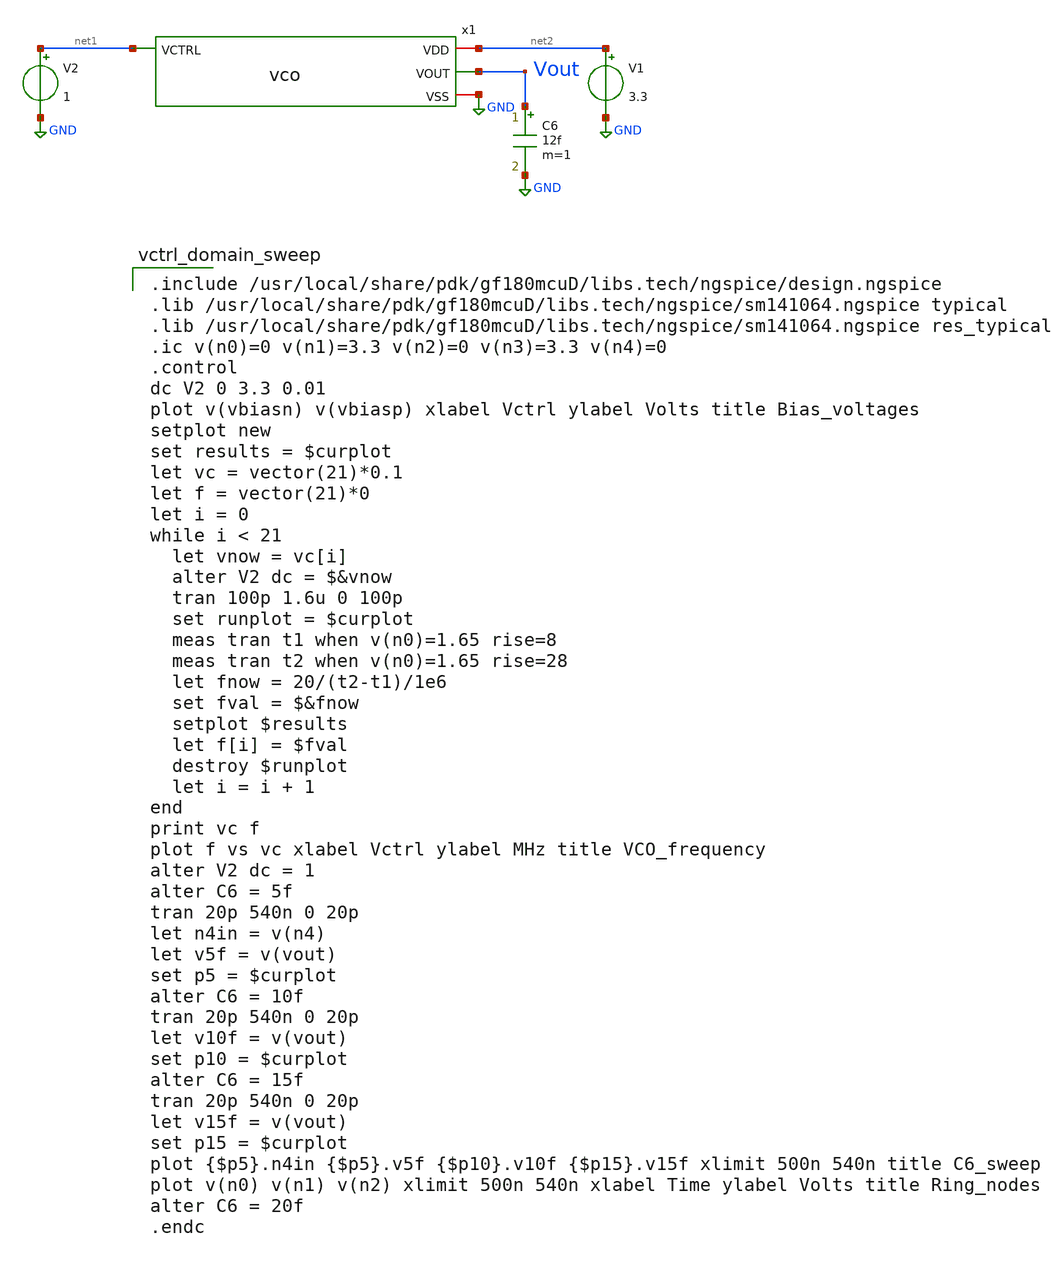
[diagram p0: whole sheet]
** sch_path: analog/vco/vco_tb.sch
**.subckt vco_tb
V1 net2 GND 3.3
V2 net1 GND 1
C6 Vout GND 12f m=1
x1 net2 net1 Vout GND vco
**** begin user architecture code

.include /usr/local/share/pdk/gf180mcuD/libs.tech/ngspice/design.ngspice
.lib /usr/local/share/pdk/gf180mcuD/libs.tech/ngspice/sm141064.ngspice typical
.lib /usr/local/share/pdk/gf180mcuD/libs.tech/ngspice/sm141064.ngspice res_typical
.ic v(n0)=0 v(n1)=3.3 v(n2)=0 v(n3)=3.3 v(n4)=0
.control
dc V2 0 3.3 0.01
plot v(vbiasn) v(vbiasp) xlabel Vctrl ylabel Volts title Bias_voltages
setplot new
set results = $curplot
let vc = vector(21)*0.1
let f = vector(21)*0
let i = 0
while i < 21
  let vnow = vc[i]
  alter V2 dc = $&vnow
  tran 100p 1.6u 0 100p
  set runplot = $curplot
  meas tran t1 when v(n0)=1.65 rise=8
  meas tran t2 when v(n0)=1.65 rise=28
  let fnow = 20/(t2-t1)/1e6
  set fval = $&fnow
  setplot $results
  let f[i] = $fval
  destroy $runplot
  let i = i + 1
end
print vc f
plot f vs vc xlabel Vctrl ylabel MHz title VCO_frequency
alter V2 dc = 1
alter C6 = 5f
tran 20p 540n 0 20p
let n4in = v(n4)
let v5f = v(vout)
set p5 = $curplot
alter C6 = 10f
tran 20p 540n 0 20p
let v10f = v(vout)
set p10 = $curplot
alter C6 = 15f
tran 20p 540n 0 20p
let v15f = v(vout)
set p15 = $curplot
plot {$p5}.n4in {$p5}.v5f {$p10}.v10f {$p15}.v15f xlimit 500n 540n title C6_sweep
plot v(n0) v(n1) v(n2) xlimit 500n 540n xlabel Time ylabel Volts title Ring_nodes
alter C6 = 20f
.endc


**** end user architecture code
**.ends

* expanding   symbol:  vco.sym # of pins=4
** sym_path: analog/vco/vco.sym
** sch_path: analog/vco/vco.sch
.subckt vco VDD VCTRL VOUT VSS
*.ipin VCTRL
*.iopin VDD
*.opin VOUT
*.iopin VSS
XM1 Vbiasn VCTRL net1 net1 pfet_03v3 L=1u W=8u nf=1 ad='int((nf+1)/2) * W/nf * 0.18u' as='int((nf+2)/2) * W/nf * 0.18u'
+ pd='2*int((nf+1)/2) * (W/nf + 0.18u)' ps='2*int((nf+2)/2) * (W/nf + 0.18u)' nrd='0.18u / W' nrs='0.18u / W'
+ sa=0 sb=0 sd=0 m=1
XM2 Vbiasn Vbiasn VSS VSS nfet_03v3 L=1u W=3u nf=1 ad='int((nf+1)/2) * W/nf * 0.18u' as='int((nf+2)/2) * W/nf * 0.18u'
+ pd='2*int((nf+1)/2) * (W/nf + 0.18u)' ps='2*int((nf+2)/2) * (W/nf + 0.18u)' nrd='0.18u / W' nrs='0.18u / W'
+ sa=0 sb=0 sd=0 m=1
XM3 Vbiasp Vbiasn VSS VSS nfet_03v3 L=1u W=3u nf=1 ad='int((nf+1)/2) * W/nf * 0.18u' as='int((nf+2)/2) * W/nf * 0.18u'
+ pd='2*int((nf+1)/2) * (W/nf + 0.18u)' ps='2*int((nf+2)/2) * (W/nf + 0.18u)' nrd='0.18u / W' nrs='0.18u / W'
+ sa=0 sb=0 sd=0 m=1
XM4 Vbiasp Vbiasp VDD VDD pfet_03v3 L=1u W=3u nf=1 ad='int((nf+1)/2) * W/nf * 0.18u' as='int((nf+2)/2) * W/nf * 0.18u'
+ pd='2*int((nf+1)/2) * (W/nf + 0.18u)' ps='2*int((nf+2)/2) * (W/nf + 0.18u)' nrd='0.18u / W' nrs='0.18u / W'
+ sa=0 sb=0 sd=0 m=1
XR1 net1 VDD VSS ppolyf_u r_width=1u r_length=189u m=1
XM5 net2 Vbiasn VSS VSS nfet_03v3 L=1u W=3u nf=1 ad='int((nf+1)/2) * W/nf * 0.18u' as='int((nf+2)/2) * W/nf * 0.18u'
+ pd='2*int((nf+1)/2) * (W/nf + 0.18u)' ps='2*int((nf+2)/2) * (W/nf + 0.18u)' nrd='0.18u / W' nrs='0.18u / W'
+ sa=0 sb=0 sd=0 m=1
XM6 n0 n4 net2 VSS nfet_03v3 L=0.28u W=1u nf=1 ad='int((nf+1)/2) * W/nf * 0.18u' as='int((nf+2)/2) * W/nf * 0.18u'
+ pd='2*int((nf+1)/2) * (W/nf + 0.18u)' ps='2*int((nf+2)/2) * (W/nf + 0.18u)' nrd='0.18u / W' nrs='0.18u / W'
+ sa=0 sb=0 sd=0 m=1
XM7 n0 n4 net3 VDD pfet_03v3 L=0.28u W=2u nf=1 ad='int((nf+1)/2) * W/nf * 0.18u' as='int((nf+2)/2) * W/nf * 0.18u'
+ pd='2*int((nf+1)/2) * (W/nf + 0.18u)' ps='2*int((nf+2)/2) * (W/nf + 0.18u)' nrd='0.18u / W' nrs='0.18u / W'
+ sa=0 sb=0 sd=0 m=1
XM8 net3 Vbiasp VDD VDD pfet_03v3 L=1u W=3u nf=1 ad='int((nf+1)/2) * W/nf * 0.18u' as='int((nf+2)/2) * W/nf * 0.18u'
+ pd='2*int((nf+1)/2) * (W/nf + 0.18u)' ps='2*int((nf+2)/2) * (W/nf + 0.18u)' nrd='0.18u / W' nrs='0.18u / W'
+ sa=0 sb=0 sd=0 m=1
XM9 net4 Vbiasn VSS VSS nfet_03v3 L=1u W=3u nf=1 ad='int((nf+1)/2) * W/nf * 0.18u' as='int((nf+2)/2) * W/nf * 0.18u'
+ pd='2*int((nf+1)/2) * (W/nf + 0.18u)' ps='2*int((nf+2)/2) * (W/nf + 0.18u)' nrd='0.18u / W' nrs='0.18u / W'
+ sa=0 sb=0 sd=0 m=1
XM10 n1 n0 net4 VSS nfet_03v3 L=0.28u W=1u nf=1 ad='int((nf+1)/2) * W/nf * 0.18u' as='int((nf+2)/2) * W/nf * 0.18u'
+ pd='2*int((nf+1)/2) * (W/nf + 0.18u)' ps='2*int((nf+2)/2) * (W/nf + 0.18u)' nrd='0.18u / W' nrs='0.18u / W'
+ sa=0 sb=0 sd=0 m=1
XM11 n1 n0 net5 VDD pfet_03v3 L=0.28u W=2u nf=1 ad='int((nf+1)/2) * W/nf * 0.18u' as='int((nf+2)/2) * W/nf * 0.18u'
+ pd='2*int((nf+1)/2) * (W/nf + 0.18u)' ps='2*int((nf+2)/2) * (W/nf + 0.18u)' nrd='0.18u / W' nrs='0.18u / W'
+ sa=0 sb=0 sd=0 m=1
XM12 net5 Vbiasp VDD VDD pfet_03v3 L=1u W=3u nf=1 ad='int((nf+1)/2) * W/nf * 0.18u' as='int((nf+2)/2) * W/nf * 0.18u'
+ pd='2*int((nf+1)/2) * (W/nf + 0.18u)' ps='2*int((nf+2)/2) * (W/nf + 0.18u)' nrd='0.18u / W' nrs='0.18u / W'
+ sa=0 sb=0 sd=0 m=1
XM13 net6 Vbiasn VSS VSS nfet_03v3 L=1u W=3u nf=1 ad='int((nf+1)/2) * W/nf * 0.18u' as='int((nf+2)/2) * W/nf * 0.18u'
+ pd='2*int((nf+1)/2) * (W/nf + 0.18u)' ps='2*int((nf+2)/2) * (W/nf + 0.18u)' nrd='0.18u / W' nrs='0.18u / W'
+ sa=0 sb=0 sd=0 m=1
XM14 n2 n1 net6 VSS nfet_03v3 L=0.28u W=1u nf=1 ad='int((nf+1)/2) * W/nf * 0.18u' as='int((nf+2)/2) * W/nf * 0.18u'
+ pd='2*int((nf+1)/2) * (W/nf + 0.18u)' ps='2*int((nf+2)/2) * (W/nf + 0.18u)' nrd='0.18u / W' nrs='0.18u / W'
+ sa=0 sb=0 sd=0 m=1
XM15 n2 n1 net7 VDD pfet_03v3 L=0.28u W=2u nf=1 ad='int((nf+1)/2) * W/nf * 0.18u' as='int((nf+2)/2) * W/nf * 0.18u'
+ pd='2*int((nf+1)/2) * (W/nf + 0.18u)' ps='2*int((nf+2)/2) * (W/nf + 0.18u)' nrd='0.18u / W' nrs='0.18u / W'
+ sa=0 sb=0 sd=0 m=1
XM16 net7 Vbiasp VDD VDD pfet_03v3 L=1u W=3u nf=1 ad='int((nf+1)/2) * W/nf * 0.18u' as='int((nf+2)/2) * W/nf * 0.18u'
+ pd='2*int((nf+1)/2) * (W/nf + 0.18u)' ps='2*int((nf+2)/2) * (W/nf + 0.18u)' nrd='0.18u / W' nrs='0.18u / W'
+ sa=0 sb=0 sd=0 m=1
XM17 net8 Vbiasn VSS VSS nfet_03v3 L=1u W=3u nf=1 ad='int((nf+1)/2) * W/nf * 0.18u' as='int((nf+2)/2) * W/nf * 0.18u'
+ pd='2*int((nf+1)/2) * (W/nf + 0.18u)' ps='2*int((nf+2)/2) * (W/nf + 0.18u)' nrd='0.18u / W' nrs='0.18u / W'
+ sa=0 sb=0 sd=0 m=1
XM18 n3 n2 net8 VSS nfet_03v3 L=0.28u W=1u nf=1 ad='int((nf+1)/2) * W/nf * 0.18u' as='int((nf+2)/2) * W/nf * 0.18u'
+ pd='2*int((nf+1)/2) * (W/nf + 0.18u)' ps='2*int((nf+2)/2) * (W/nf + 0.18u)' nrd='0.18u / W' nrs='0.18u / W'
+ sa=0 sb=0 sd=0 m=1
XM19 n3 n2 net9 VDD pfet_03v3 L=0.28u W=2u nf=1 ad='int((nf+1)/2) * W/nf * 0.18u' as='int((nf+2)/2) * W/nf * 0.18u'
+ pd='2*int((nf+1)/2) * (W/nf + 0.18u)' ps='2*int((nf+2)/2) * (W/nf + 0.18u)' nrd='0.18u / W' nrs='0.18u / W'
+ sa=0 sb=0 sd=0 m=1
XM20 net9 Vbiasp VDD VDD pfet_03v3 L=1u W=3u nf=1 ad='int((nf+1)/2) * W/nf * 0.18u' as='int((nf+2)/2) * W/nf * 0.18u'
+ pd='2*int((nf+1)/2) * (W/nf + 0.18u)' ps='2*int((nf+2)/2) * (W/nf + 0.18u)' nrd='0.18u / W' nrs='0.18u / W'
+ sa=0 sb=0 sd=0 m=1
XM21 net10 Vbiasn VSS VSS nfet_03v3 L=1u W=3u nf=1 ad='int((nf+1)/2) * W/nf * 0.18u' as='int((nf+2)/2) * W/nf * 0.18u'
+ pd='2*int((nf+1)/2) * (W/nf + 0.18u)' ps='2*int((nf+2)/2) * (W/nf + 0.18u)' nrd='0.18u / W' nrs='0.18u / W'
+ sa=0 sb=0 sd=0 m=1
XM22 n4 n3 net10 VSS nfet_03v3 L=0.28u W=1u nf=1 ad='int((nf+1)/2) * W/nf * 0.18u' as='int((nf+2)/2) * W/nf * 0.18u'
+ pd='2*int((nf+1)/2) * (W/nf + 0.18u)' ps='2*int((nf+2)/2) * (W/nf + 0.18u)' nrd='0.18u / W' nrs='0.18u / W'
+ sa=0 sb=0 sd=0 m=1
XM23 n4 n3 net11 VDD pfet_03v3 L=0.28u W=2u nf=1 ad='int((nf+1)/2) * W/nf * 0.18u' as='int((nf+2)/2) * W/nf * 0.18u'
+ pd='2*int((nf+1)/2) * (W/nf + 0.18u)' ps='2*int((nf+2)/2) * (W/nf + 0.18u)' nrd='0.18u / W' nrs='0.18u / W'
+ sa=0 sb=0 sd=0 m=1
XM24 net11 Vbiasp VDD VDD pfet_03v3 L=1u W=3u nf=1 ad='int((nf+1)/2) * W/nf * 0.18u' as='int((nf+2)/2) * W/nf * 0.18u'
+ pd='2*int((nf+1)/2) * (W/nf + 0.18u)' ps='2*int((nf+2)/2) * (W/nf + 0.18u)' nrd='0.18u / W' nrs='0.18u / W'
+ sa=0 sb=0 sd=0 m=1
C1 n0 VSS 3f m=1
C2 n1 VSS 3f m=1
C3 n2 VSS 3f m=1
C4 n3 VSS 3f m=1
C5 n4 VSS 3f m=1
XM25 net12 n4 VSS VSS nfet_03v3 L=0.28u W=1u nf=1 ad='int((nf+1)/2) * W/nf * 0.18u' as='int((nf+2)/2) * W/nf * 0.18u'
+ pd='2*int((nf+1)/2) * (W/nf + 0.18u)' ps='2*int((nf+2)/2) * (W/nf + 0.18u)' nrd='0.18u / W' nrs='0.18u / W'
+ sa=0 sb=0 sd=0 m=1
XM26 net12 n4 VDD VDD pfet_03v3 L=0.28u W=2u nf=1 ad='int((nf+1)/2) * W/nf * 0.18u' as='int((nf+2)/2) * W/nf * 0.18u'
+ pd='2*int((nf+1)/2) * (W/nf + 0.18u)' ps='2*int((nf+2)/2) * (W/nf + 0.18u)' nrd='0.18u / W' nrs='0.18u / W'
+ sa=0 sb=0 sd=0 m=1
XM27 VOUT net12 VSS VSS nfet_03v3 L=0.28u W=1u nf=1 ad='int((nf+1)/2) * W/nf * 0.18u' as='int((nf+2)/2) * W/nf * 0.18u'
+ pd='2*int((nf+1)/2) * (W/nf + 0.18u)' ps='2*int((nf+2)/2) * (W/nf + 0.18u)' nrd='0.18u / W' nrs='0.18u / W'
+ sa=0 sb=0 sd=0 m=1
XM28 VOUT net12 VDD VDD pfet_03v3 L=0.28u W=2u nf=1 ad='int((nf+1)/2) * W/nf * 0.18u' as='int((nf+2)/2) * W/nf * 0.18u'
+ pd='2*int((nf+1)/2) * (W/nf + 0.18u)' ps='2*int((nf+2)/2) * (W/nf + 0.18u)' nrd='0.18u / W' nrs='0.18u / W'
+ sa=0 sb=0 sd=0 m=1
C7 net12 VSS 3f m=1
.ends

.GLOBAL GND
.end
